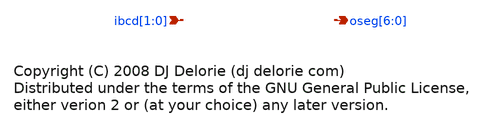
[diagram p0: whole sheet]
** sch_path: xschem_libs_newsym/binto7seg/sevenseg012/schematic/sevenseg012.sch
* Copyright (C) 1998-2024 Stefan Frederik Schippers
* This program is free software; you can redistribute it and/or modify
* it under the terms of the GNU General Public License as published by
* the Free Software Foundation; either version 2 of the License, or
* (at your option) any later version.
* This program is distributed in the hope that it will be useful,
* but WITHOUT ANY WARRANTY; without even the implied warranty of
* MERCHANTABILITY or FITNESS FOR A PARTICULAR PURPOSE.  See the
* GNU General Public License for more details.
* You should have received a copy of the GNU General Public License
* along with this program; if not, write to the Free Software
**.subckt sevenseg012 ibcd[1],ibcd[0] oseg[6],oseg[5],oseg[4],oseg[3],oseg[2],oseg[1],oseg[0]
*.ipin ibcd[1],ibcd[0]
*.opin oseg[6],oseg[5],oseg[4],oseg[3],oseg[2],oseg[1],oseg[0]
**** begin user architecture code

// Copyright (C) 2008 DJ Delorie <dj delorie com>
// Distributed under the terms of the GNU General Public License,
// either verion 2 or (at your choice) any later version.

always @ (ibcd)
begin
  case (ibcd)  // abcdefg
    0 : oseg = 7'b1111110;
    1 : oseg = 7'b0110000;
    2 : oseg = 7'b1101101;
    default : oseg = 0;
  endcase
end


**** end user architecture code
**.ends
.end
